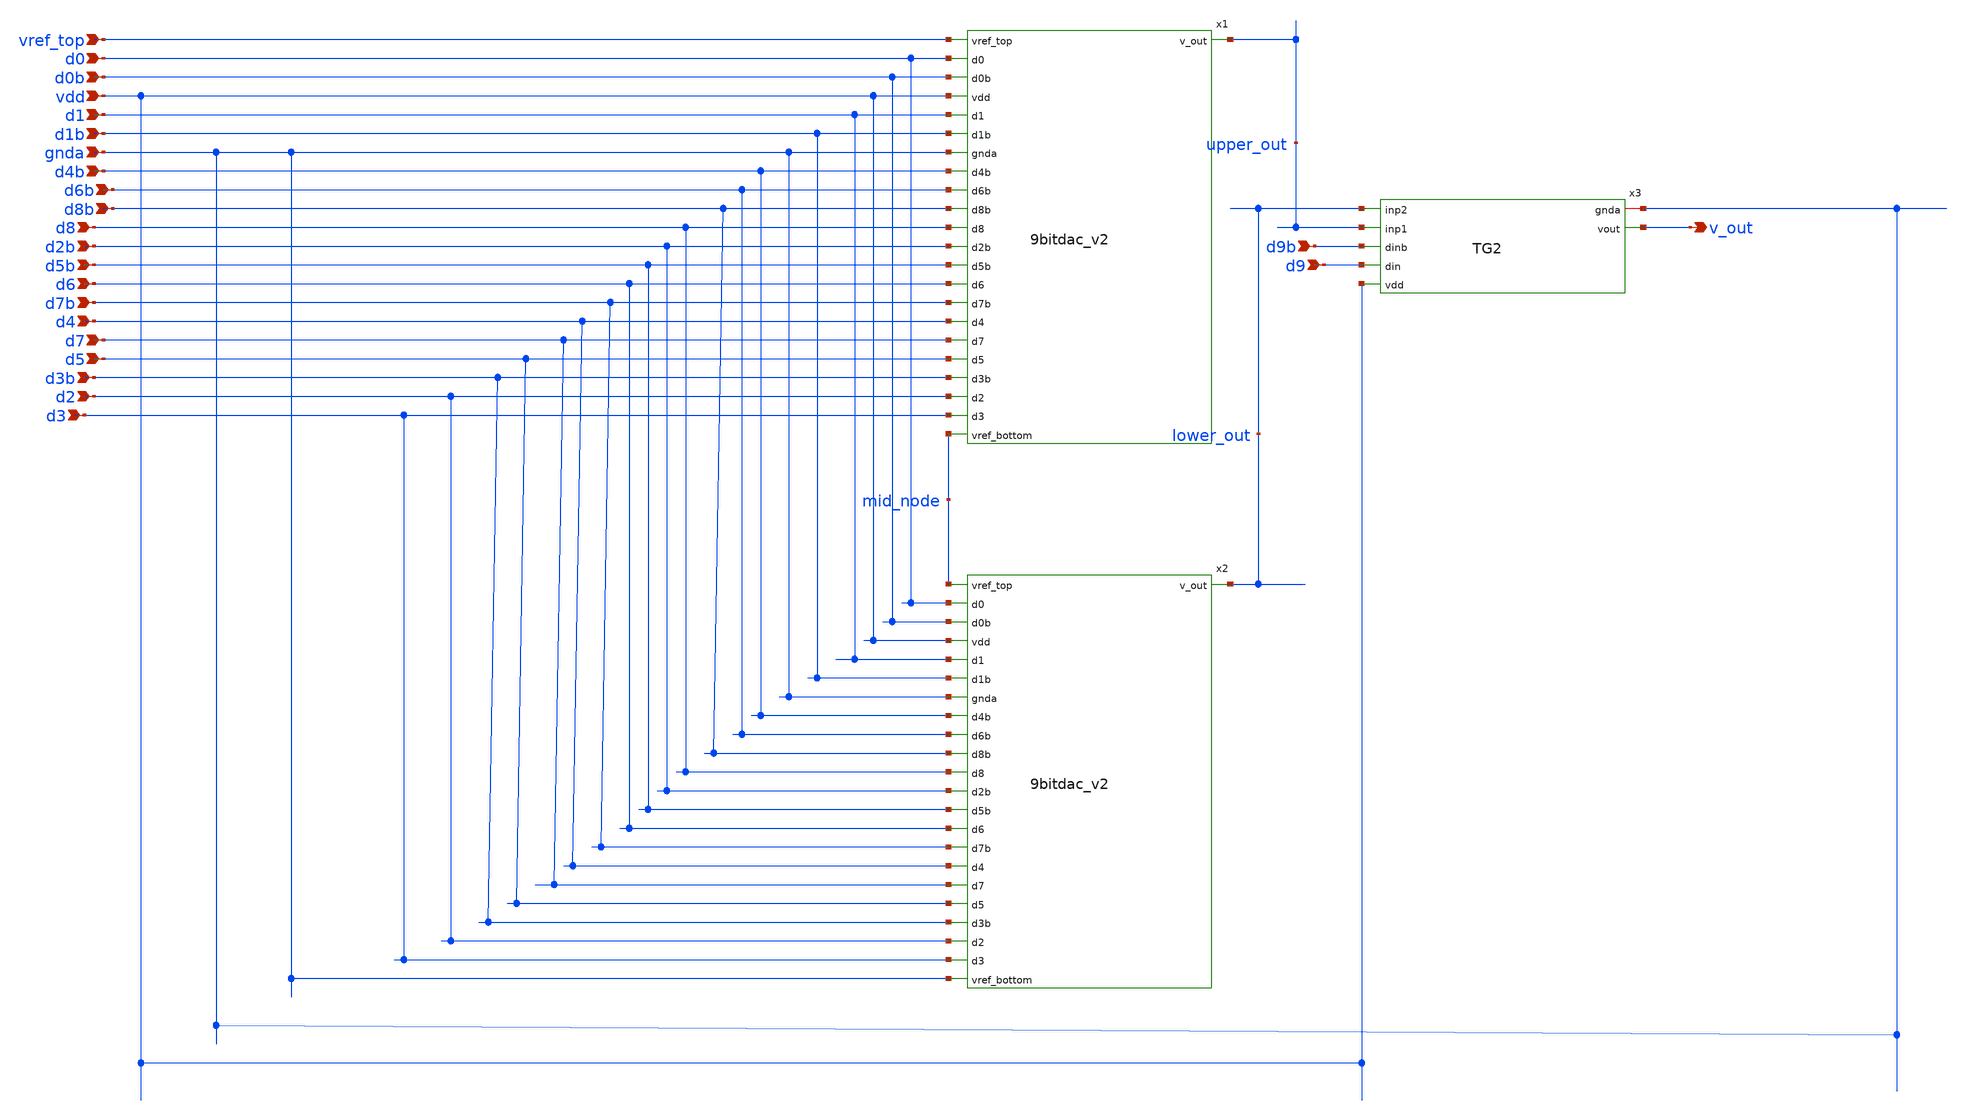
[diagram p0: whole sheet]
** sch_path: prelayout/10bitdac.sch
**.subckt 10bitdac vref_top d0 d0b vdd d1 d1b gnda d4b d6b d8b d8 d2b d5b d6 d7b d4 d7 d5 d3b d2 d3
*+ d9b d9 v_out
*.ipin vref_top
*.ipin d0
*.ipin d0b
*.ipin vdd
*.ipin d1
*.ipin d1b
*.ipin gnda
*.ipin d4b
*.ipin d6b
*.ipin d8b
*.ipin d8
*.ipin d2b
*.ipin d5b
*.ipin d6
*.ipin d7b
*.ipin d4
*.ipin d7
*.ipin d5
*.ipin d3b
*.ipin d2
*.ipin d3
*.ipin d9b
*.ipin d9
*.opin v_out
x1 vref_top d0 d0b vdd d1 d1b gnda d4b upper_out d6b d8b d8 d2b d5b d6 d7b d4 d7 d5 d3b d2 d3
+ mid_node 9bitdac_v2
x2 mid_node d0 d0b vdd d1 d1b gnda d4b lower_out d6b d8b d8 d2b d5b d6 d7b d4 d7 d5 d3b d2 d3 gnda
+ 9bitdac_v2
Xx3 gnda v_out lower_out upper_out d9b d9 vdd TG2
**.ends
.end
